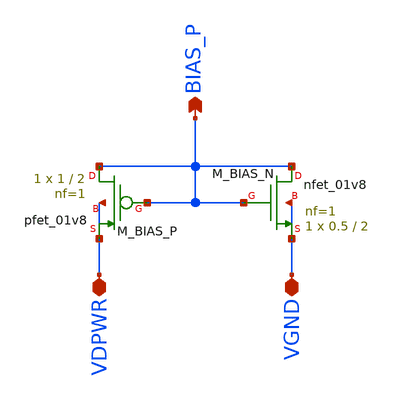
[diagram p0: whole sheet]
** sch_path: xschem/bias_gen.sch
**.subckt bias_gen VDPWR VGND BIAS_P
*.iopin VDPWR
*.iopin VGND
*.opin BIAS_P
XM_BIAS_P BIAS_P BIAS_P VDPWR VDPWR sky130_fd_pr__pfet_01v8 L=2 W=1 nf=1 ad='int((1 + 1)/2) * 1 / 1 * 0.29'
+ as='int((1 + 2)/2) * 1 / 1 * 0.29' pd='2*int((1 + 1)/2) * (1 / 1 + 0.29)' ps='2*int((1 + 2)/2) * (1 / 1 + 0.29)'
+ nrd='0.29 / 1 ' nrs='0.29 / 1 ' sa=0 sb=0 sd=0 mult=1 m=1
XM_BIAS_N BIAS_P BIAS_P VGND VGND sky130_fd_pr__nfet_01v8 L=2 W=0.5 nf=1 ad='int((1 + 1)/2) * 0.5 / 1 * 0.29'
+ as='int((1 + 2)/2) * 0.5 / 1 * 0.29' pd='2*int((1 + 1)/2) * (0.5 / 1 + 0.29)' ps='2*int((1 + 2)/2) * (0.5 / 1 + 0.29)'
+ nrd='0.29 / 0.5 ' nrs='0.29 / 0.5 ' sa=0 sb=0 sd=0 mult=1 m=1
**.ends
.end
